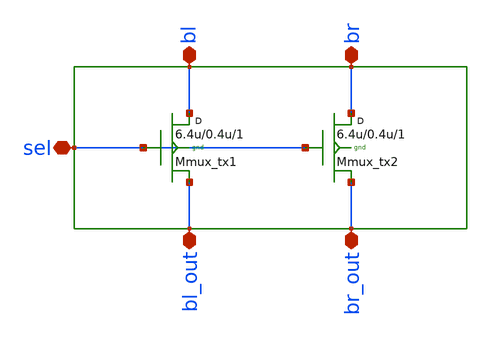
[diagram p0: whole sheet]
** sch_path: sram_2_64_scn4m_lcc/column_mux.sch
**.subckt column_mux bl br sel bl_out br_out
*.iopin bl
*.iopin br
*.iopin sel
*.iopin bl_out
*.iopin br_out
Mmux_tx1 bl sel bl_out gnd n w=6.4u l=0.4u m=1
Mmux_tx2 br sel br_out gnd n w=6.4u l=0.4u m=1
**.ends
.end
